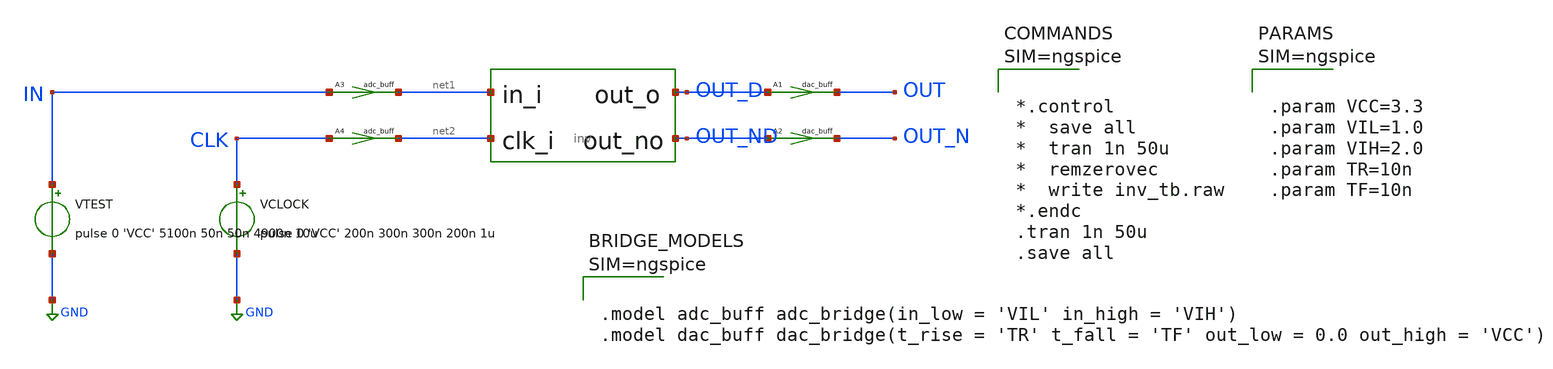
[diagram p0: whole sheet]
** sch_path: inv_tb.sch
**.subckt inv_tb
ADUT [ net2 net1 ] [ OUT_D OUT_ND ] dut
VCLOCK CLK GND pulse 0 'VCC' 200n 300n 300n 200n 1u
VTEST IN GND pulse 0 'VCC' 5100n 50n 50n 4900n 10u
A1 [ OUT_D ] [ OUT ] dac_buff
A2 [ OUT_ND ] [ OUT_N ] dac_buff
A3 [ IN ] [ net1 ] adc_buff
A4 [ CLK ] [ net2 ] adc_buff
**** begin user architecture code



*.control
*  save all
*  tran 1n 50u
*  remzerovec
*  write inv_tb.raw
*.endc
.tran 1n 50u
.save all






.param VCC=3.3
.param VIL=1.0
.param VIH=2.0
.param TR=10n
.param TF=10n






.model adc_buff adc_bridge(in_low = 'VIL' in_high = 'VIH')
.model dac_buff dac_bridge(t_rise = 'TR' t_fall = 'TF' out_low = 0.0 out_high = 'VCC')



**** end user architecture code
**.ends
.GLOBAL GND
**** begin user architecture code
.model dut d_cosim simulation="ivlng" sim_args=["inv"]
**** end user architecture code
.end
